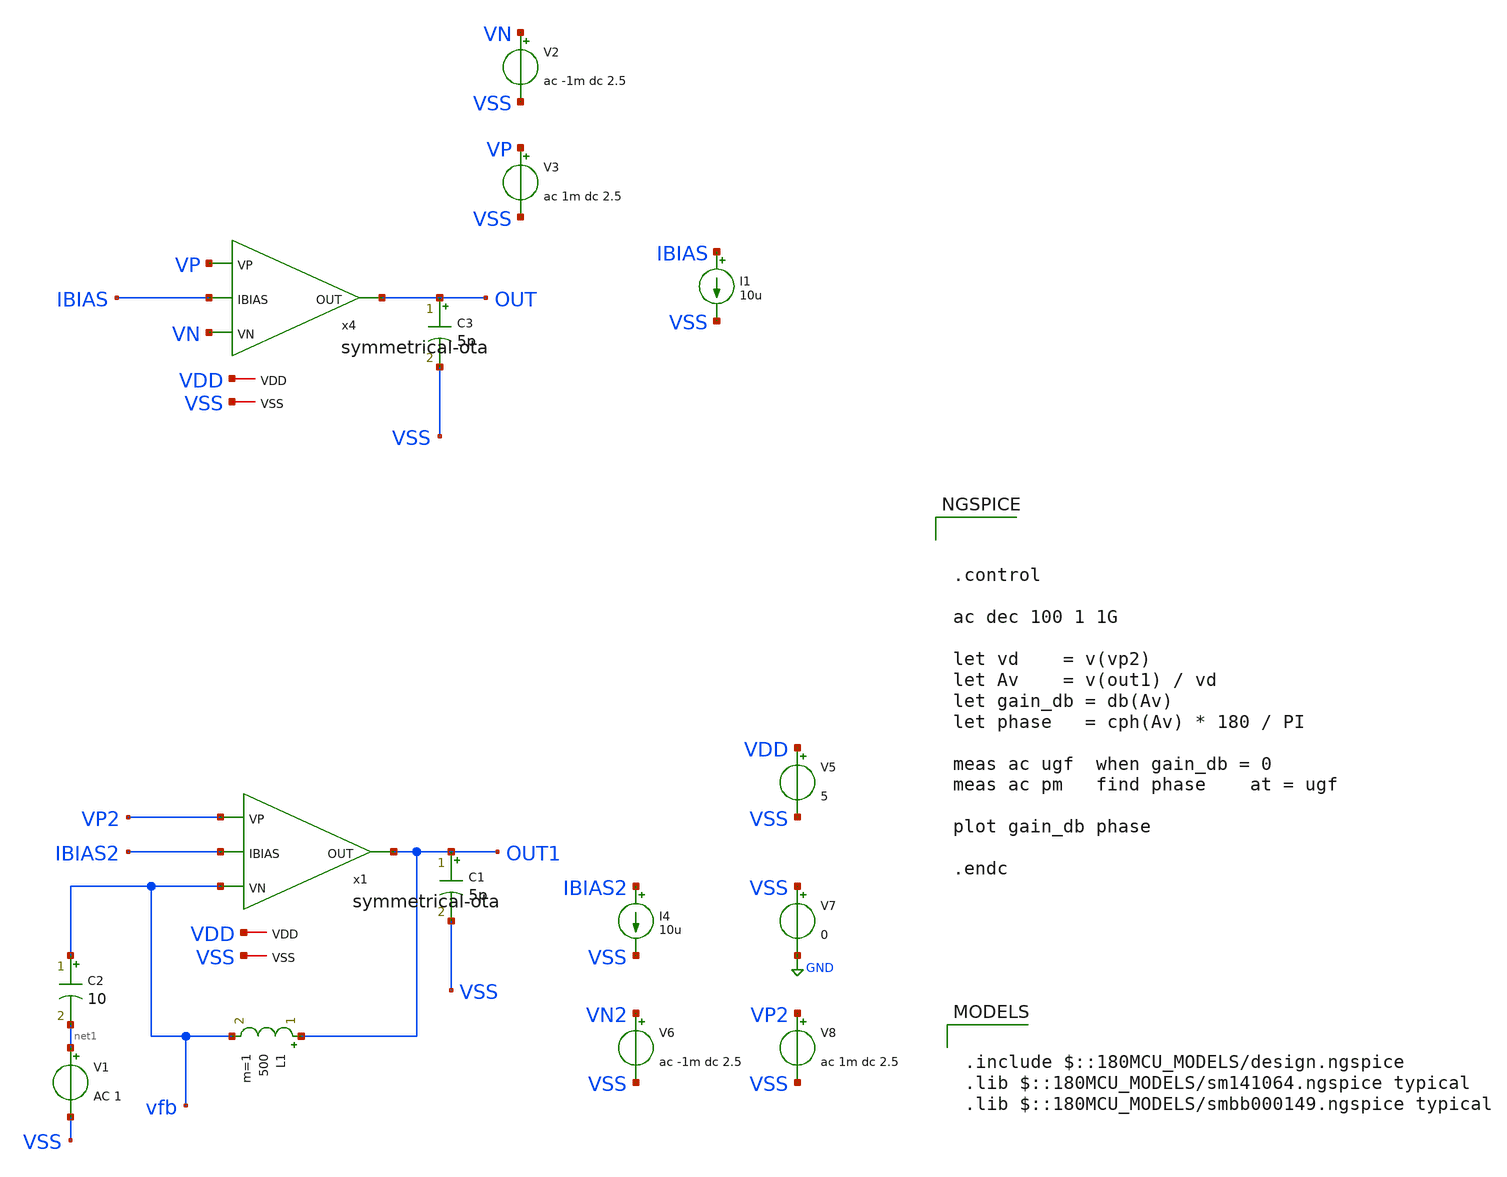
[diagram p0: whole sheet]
** sch_path: designs/symmetrical-ota/tb-ac.sch
**.subckt tb-ac
V2 VN VSS ac -1m dc 2.5
V3 VP VSS ac 1m dc 2.5
V5 VDD VSS 5
V7 VSS GND 0
I4 IBIAS2 VSS 10u
C3 OUT VSS 5p m=1
x4 VDD VP VN IBIAS OUT VSS symmetrical-ota
C1 OUT1 VSS 5p m=1
x1 VDD VP2 vfb IBIAS2 OUT1 VSS symmetrical-ota
L1 OUT1 vfb 500 m=1
V6 VN2 VSS ac -1m dc 2.5
V8 VP2 VSS ac 1m dc 2.5
I1 IBIAS VSS 10u
C2 vfb net1 10 m=1
V1 net1 VSS AC 1
**** begin user architecture code



.control

ac dec 100 1 1G

let vd    = v(vp2)
let Av    = v(out1) / vd
let gain_db = db(Av)
let phase   = cph(Av) * 180 / PI

meas ac ugf  when gain_db = 0
meas ac pm   find phase    at = ugf

plot gain_db phase

.endc




.include $::180MCU_MODELS/design.ngspice
.lib $::180MCU_MODELS/sm141064.ngspice typical
.lib $::180MCU_MODELS/smbb000149.ngspice typical

**** end user architecture code
**.ends

* expanding   symbol:
*+  /foss/designs/2026/buck-gf180-test/designs/symmetrical-ota/symmetrical-ota.sym # of pins=6
** sym_path: designs/symmetrical-ota/symmetrical-ota.sym
** sch_path: designs/symmetrical-ota/symmetrical-ota.sch
.subckt symmetrical-ota VDD VP VN IBIAS OUT VSS
*.ipin IBIAS
*.ipin VN
*.ipin VP
*.opin OUT
*.iopin VDD
*.iopin VSS
XM1 net3 VN net1 VDD pfet_05v0 L=0.9u W=10.5u nf=4 ad='int((nf+1)/2) * W/nf * 0.18u' as='int((nf+2)/2) * W/nf * 0.18u'
+ pd='2*int((nf+1)/2) * (W/nf + 0.18u)' ps='2*int((nf+2)/2) * (W/nf + 0.18u)' nrd='0.18u / W' nrs='0.18u / W'
+ sa=0 sb=0 sd=0 m=1
XM2 net2 VP net1 VDD pfet_05v0 L=0.9u W=10.5u nf=4 ad='int((nf+1)/2) * W/nf * 0.18u' as='int((nf+2)/2) * W/nf * 0.18u'
+ pd='2*int((nf+1)/2) * (W/nf + 0.18u)' ps='2*int((nf+2)/2) * (W/nf + 0.18u)' nrd='0.18u / W' nrs='0.18u / W'
+ sa=0 sb=0 sd=0 m=1
XM3 net1 IBIAS VDD VDD pfet_05v0 L=1u W=15u nf=4 ad='int((nf+1)/2) * W/nf * 0.18u' as='int((nf+2)/2) * W/nf * 0.18u'
+ pd='2*int((nf+1)/2) * (W/nf + 0.18u)' ps='2*int((nf+2)/2) * (W/nf + 0.18u)' nrd='0.18u / W' nrs='0.18u / W'
+ sa=0 sb=0 sd=0 m=1
XM4 IBIAS IBIAS VDD VDD pfet_05v0 L=1u W=15u nf=4 ad='int((nf+1)/2) * W/nf * 0.18u' as='int((nf+2)/2) * W/nf * 0.18u'
+ pd='2*int((nf+1)/2) * (W/nf + 0.18u)' ps='2*int((nf+2)/2) * (W/nf + 0.18u)' nrd='0.18u / W' nrs='0.18u / W'
+ sa=0 sb=0 sd=0 m=1
XM5 net2 net2 VSS VSS nfet_05v0 L=0.75u W=2.17u nf=1 ad='int((nf+1)/2) * W/nf * 0.18u' as='int((nf+2)/2) * W/nf * 0.18u'
+ pd='2*int((nf+1)/2) * (W/nf + 0.18u)' ps='2*int((nf+2)/2) * (W/nf + 0.18u)' nrd='0.18u / W' nrs='0.18u / W'
+ sa=0 sb=0 sd=0 m=1
XM6 net3 net3 VSS VSS nfet_05v0 L=0.75u W=2.17u nf=1 ad='int((nf+1)/2) * W/nf * 0.18u' as='int((nf+2)/2) * W/nf * 0.18u'
+ pd='2*int((nf+1)/2) * (W/nf + 0.18u)' ps='2*int((nf+2)/2) * (W/nf + 0.18u)' nrd='0.18u / W' nrs='0.18u / W'
+ sa=0 sb=0 sd=0 m=1
XM7 OUT net4 VDD VDD pfet_05v0 L=1u W=9.4u nf=4 ad='int((nf+1)/2) * W/nf * 0.18u' as='int((nf+2)/2) * W/nf * 0.18u'
+ pd='2*int((nf+1)/2) * (W/nf + 0.18u)' ps='2*int((nf+2)/2) * (W/nf + 0.18u)' nrd='0.18u / W' nrs='0.18u / W'
+ sa=0 sb=0 sd=0 m=1
XM8 net4 net4 VDD VDD pfet_05v0 L=1u W=9.4u nf=4 ad='int((nf+1)/2) * W/nf * 0.18u' as='int((nf+2)/2) * W/nf * 0.18u'
+ pd='2*int((nf+1)/2) * (W/nf + 0.18u)' ps='2*int((nf+2)/2) * (W/nf + 0.18u)' nrd='0.18u / W' nrs='0.18u / W'
+ sa=0 sb=0 sd=0 m=1
XM9 net4 net3 VSS VSS nfet_05v0 L=0.75u W=2.17u nf=1 ad='int((nf+1)/2) * W/nf * 0.18u' as='int((nf+2)/2) * W/nf * 0.18u'
+ pd='2*int((nf+1)/2) * (W/nf + 0.18u)' ps='2*int((nf+2)/2) * (W/nf + 0.18u)' nrd='0.18u / W' nrs='0.18u / W'
+ sa=0 sb=0 sd=0 m=1
XM10 OUT net2 VSS VSS nfet_05v0 L=0.75u W=2.17u nf=1 ad='int((nf+1)/2) * W/nf * 0.18u' as='int((nf+2)/2) * W/nf * 0.18u'
+ pd='2*int((nf+1)/2) * (W/nf + 0.18u)' ps='2*int((nf+2)/2) * (W/nf + 0.18u)' nrd='0.18u / W' nrs='0.18u / W'
+ sa=0 sb=0 sd=0 m=1
.ends

.GLOBAL GND
.end
